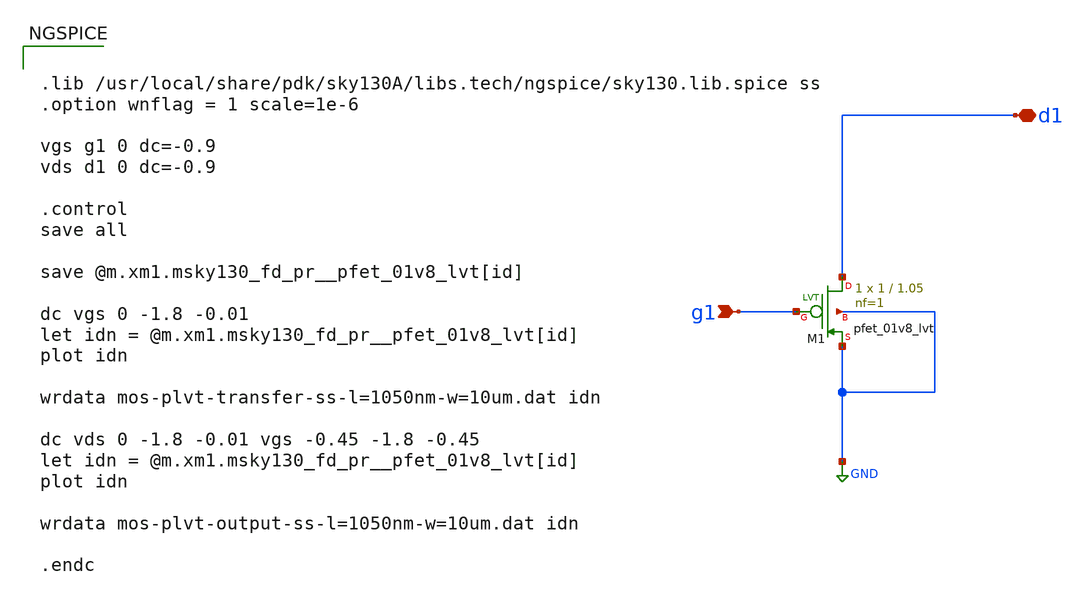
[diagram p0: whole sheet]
** sch_path: MOS-Transistor-Characteristics/act4p.sch
**.subckt act4p g1 d1
*.ipin g1
*.iopin d1
XM1 d1 g1 GND GND sky130_fd_pr__pfet_01v8_lvt L=1.05 W=1 nf=1 ad='int((nf+1)/2) * W/nf * 0.29' as='int((nf+2)/2) * W/nf * 0.29'
+ pd='2*int((nf+1)/2) * (W/nf + 0.29)' ps='2*int((nf+2)/2) * (W/nf + 0.29)' nrd='0.29 / W' nrs='0.29 / W'
+ sa=0 sb=0 sd=0 mult=1 m=1
**** begin user architecture code


.lib /usr/local/share/pdk/sky130A/libs.tech/ngspice/sky130.lib.spice ss
.option wnflag = 1 scale=1e-6

vgs g1 0 dc=-0.9
vds d1 0 dc=-0.9

.control
save all

save @m.xm1.msky130_fd_pr__pfet_01v8_lvt[id]

dc vgs 0 -1.8 -0.01
let idn = @m.xm1.msky130_fd_pr__pfet_01v8_lvt[id]
plot idn

wrdata mos-plvt-transfer-ss-l=1050nm-w=10um.dat idn

dc vds 0 -1.8 -0.01 vgs -0.45 -1.8 -0.45
let idn = @m.xm1.msky130_fd_pr__pfet_01v8_lvt[id]
plot idn

wrdata mos-plvt-output-ss-l=1050nm-w=10um.dat idn

.endc


**** end user architecture code
**.ends
.GLOBAL GND
.end
